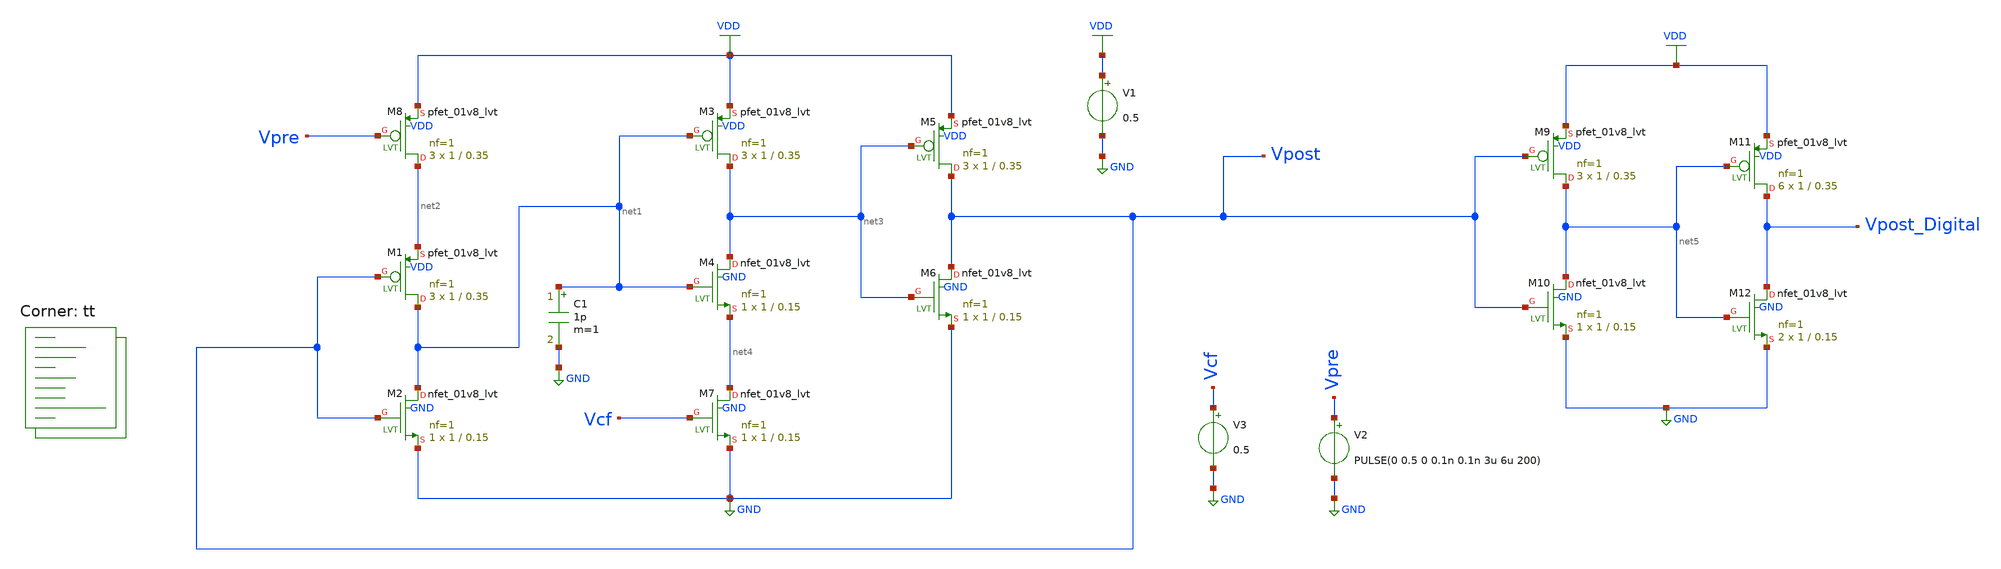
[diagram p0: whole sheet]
** sch_path: xschem/LPCAS_LIF.sch
**.subckt LPCAS_LIF
XM1 net1 Vpost net2 VDD sky130_fd_pr__pfet_01v8_lvt L=0.35 W=1 nf=1 ad='int((nf+1)/2) * W/nf * 0.29'
+ as='int((nf+2)/2) * W/nf * 0.29' pd='2*int((nf+1)/2) * (W/nf + 0.29)' ps='2*int((nf+2)/2) * (W/nf + 0.29)'
+ nrd='0.29 / W' nrs='0.29 / W' sa=0 sb=0 sd=0 mult=3 m=3
XM2 net1 Vpost GND GND sky130_fd_pr__nfet_01v8_lvt L=0.15 W=1 nf=1 ad='int((nf+1)/2) * W/nf * 0.29' as='int((nf+2)/2) * W/nf * 0.29'
+ pd='2*int((nf+1)/2) * (W/nf + 0.29)' ps='2*int((nf+2)/2) * (W/nf + 0.29)' nrd='0.29 / W' nrs='0.29 / W'
+ sa=0 sb=0 sd=0 mult=1 m=1
XM3 net3 net1 VDD VDD sky130_fd_pr__pfet_01v8_lvt L=0.35 W=1 nf=1 ad='int((nf+1)/2) * W/nf * 0.29' as='int((nf+2)/2) * W/nf * 0.29'
+ pd='2*int((nf+1)/2) * (W/nf + 0.29)' ps='2*int((nf+2)/2) * (W/nf + 0.29)' nrd='0.29 / W' nrs='0.29 / W'
+ sa=0 sb=0 sd=0 mult=3 m=3
XM4 net3 net1 net4 GND sky130_fd_pr__nfet_01v8_lvt L=0.15 W=1 nf=1 ad='int((nf+1)/2) * W/nf * 0.29' as='int((nf+2)/2) * W/nf * 0.29'
+ pd='2*int((nf+1)/2) * (W/nf + 0.29)' ps='2*int((nf+2)/2) * (W/nf + 0.29)' nrd='0.29 / W' nrs='0.29 / W'
+ sa=0 sb=0 sd=0 mult=1 m=1
XM5 Vpost net3 VDD VDD sky130_fd_pr__pfet_01v8_lvt L=0.35 W=1 nf=1 ad='int((nf+1)/2) * W/nf * 0.29' as='int((nf+2)/2) * W/nf * 0.29'
+ pd='2*int((nf+1)/2) * (W/nf + 0.29)' ps='2*int((nf+2)/2) * (W/nf + 0.29)' nrd='0.29 / W' nrs='0.29 / W'
+ sa=0 sb=0 sd=0 mult=3 m=3
XM6 Vpost net3 GND GND sky130_fd_pr__nfet_01v8_lvt L=0.15 W=1 nf=1 ad='int((nf+1)/2) * W/nf * 0.29' as='int((nf+2)/2) * W/nf * 0.29'
+ pd='2*int((nf+1)/2) * (W/nf + 0.29)' ps='2*int((nf+2)/2) * (W/nf + 0.29)' nrd='0.29 / W' nrs='0.29 / W'
+ sa=0 sb=0 sd=0 mult=1 m=1
XM7 net4 Vcf GND GND sky130_fd_pr__nfet_01v8_lvt L=0.15 W=1 nf=1 ad='int((nf+1)/2) * W/nf * 0.29' as='int((nf+2)/2) * W/nf * 0.29'
+ pd='2*int((nf+1)/2) * (W/nf + 0.29)' ps='2*int((nf+2)/2) * (W/nf + 0.29)' nrd='0.29 / W' nrs='0.29 / W'
+ sa=0 sb=0 sd=0 mult=1 m=1
XM8 net2 Vpre VDD VDD sky130_fd_pr__pfet_01v8_lvt L=0.35 W=1 nf=1 ad='int((nf+1)/2) * W/nf * 0.29' as='int((nf+2)/2) * W/nf * 0.29'
+ pd='2*int((nf+1)/2) * (W/nf + 0.29)' ps='2*int((nf+2)/2) * (W/nf + 0.29)' nrd='0.29 / W' nrs='0.29 / W'
+ sa=0 sb=0 sd=0 mult=3 m=3
V1 VDD GND 0.5
C1 net1 GND 1p m=1
V2 Vpre GND PULSE(0 0.5 0 0.1n 0.1n 3u 6u 200)
V3 Vcf GND 0.5
XM9 net5 Vpost VDD VDD sky130_fd_pr__pfet_01v8_lvt L=0.35 W=1 nf=1 ad='int((nf+1)/2) * W/nf * 0.29' as='int((nf+2)/2) * W/nf * 0.29'
+ pd='2*int((nf+1)/2) * (W/nf + 0.29)' ps='2*int((nf+2)/2) * (W/nf + 0.29)' nrd='0.29 / W' nrs='0.29 / W'
+ sa=0 sb=0 sd=0 mult=3 m=3
XM10 net5 Vpost GND GND sky130_fd_pr__nfet_01v8_lvt L=0.15 W=1 nf=1 ad='int((nf+1)/2) * W/nf * 0.29'
+ as='int((nf+2)/2) * W/nf * 0.29' pd='2*int((nf+1)/2) * (W/nf + 0.29)' ps='2*int((nf+2)/2) * (W/nf + 0.29)'
+ nrd='0.29 / W' nrs='0.29 / W' sa=0 sb=0 sd=0 mult=1 m=1
XM11 Vpost_Digital net5 VDD VDD sky130_fd_pr__pfet_01v8_lvt L=0.35 W=1 nf=1 ad='int((nf+1)/2) * W/nf * 0.29'
+ as='int((nf+2)/2) * W/nf * 0.29' pd='2*int((nf+1)/2) * (W/nf + 0.29)' ps='2*int((nf+2)/2) * (W/nf + 0.29)'
+ nrd='0.29 / W' nrs='0.29 / W' sa=0 sb=0 sd=0 mult=6 m=6
XM12 Vpost_Digital net5 GND GND sky130_fd_pr__nfet_01v8_lvt L=0.15 W=1 nf=1 ad='int((nf+1)/2) * W/nf * 0.29'
+ as='int((nf+2)/2) * W/nf * 0.29' pd='2*int((nf+1)/2) * (W/nf + 0.29)' ps='2*int((nf+2)/2) * (W/nf + 0.29)'
+ nrd='0.29 / W' nrs='0.29 / W' sa=0 sb=0 sd=0 mult=2 m=2
**** begin user architecture code



.include /foss/pdks/volare/sky130/versions/0fe599b2afb6708d281543108caf8310912f54af/sky130A/libs.ref/sky130_fd_sc_hd/spice/sky130_fd_sc_hd.spice tt
.option wnflag=1
.option savecurrents
.temp 27

.control
save all
write LPCAS_LIF.raw
set appendwrite
op
write LPCAS_LIF.raw
tran 10n 200u uic
plot v(vpost) v(vpre)
plot v(vpost) v(vpre) v(vpost_digital)
**wrdata /foss/designs/LIF/LIF-Tapeout/fft_data_VCF_1_8_tran_1p.txt v(vpost) v(vpre)
*+ v(vpost_digital)

* Perform FFT
fft v(vpost)
plot mag(v(vpost))

* Save FFT to file to find peak frequency
wrdata /foss/designs/LIF/LIF-Tapeout/fft_data_VCF_1_8_fft_1p.txt mag(v(vpost))

.endc



.lib $::SKYWATER_MODELS/sky130.lib.spice tt
**** end user architecture code
**.ends
.GLOBAL GND
.GLOBAL VDD
.end
